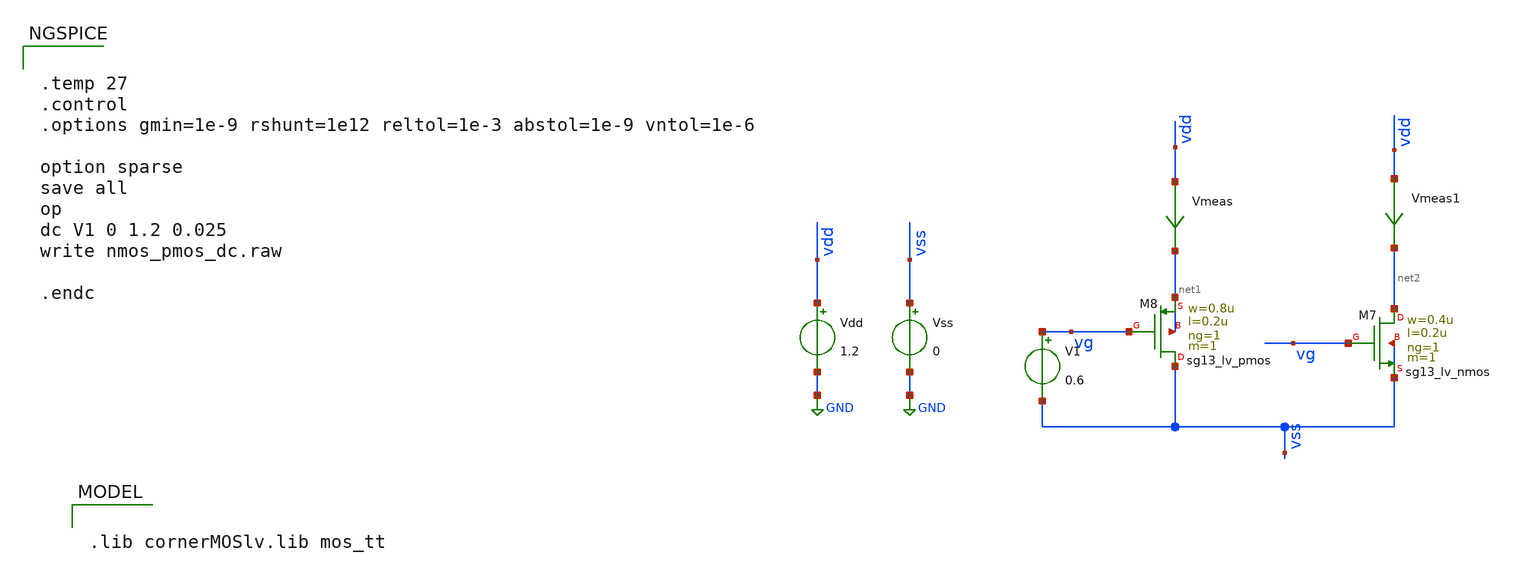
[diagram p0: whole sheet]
** sch_path: v2_feature_extr/nmos_pmos_dc.sch
**.subckt nmos_pmos_dc
XM7 net2 vg vss vss sg13_lv_nmos w=0.4u l=0.2u ng=1 m=1 mm_ok=1
XM8 vss vg net1 net1 sg13_lv_pmos w=0.8u l=0.2u ng=1 m=1 mm_ok=1
Vdd vdd GND 1.2
Vss vss GND 0
Vmeas vdd net1 0
.save i(vmeas)
Vmeas1 vdd net2 0
.save i(vmeas1)
V1 vg vss 0.6
**** begin user architecture code


.temp 27
.control
.options gmin=1e-9 rshunt=1e12 reltol=1e-3 abstol=1e-9 vntol=1e-6

option sparse
save all
op
dc V1 0 1.2 0.025
write nmos_pmos_dc.raw

.endc



.lib cornerMOSlv.lib mos_tt

**** end user architecture code
**.ends
.GLOBAL GND
.end
